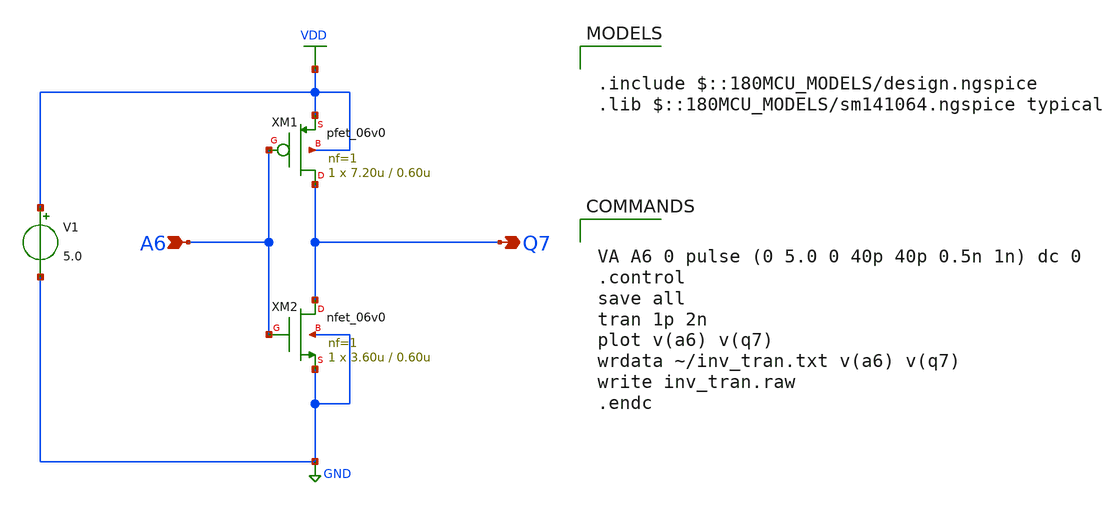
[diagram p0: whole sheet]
** sch_path: member_project/noritsuna/inverter/xschem/inverter_trans.sch
**.subckt inverter_trans A6 Q7
*.ipin A6
*.opin Q7
XM1 Q7 A6 VDD VDD pfet_06v0 L=0.60u W=7.20u nf=1 ad='int((nf+1)/2) * W/nf * 0.18u' as='int((nf+2)/2) * W/nf * 0.18u'
+ pd='2*int((nf+1)/2) * (W/nf + 0.18u)' ps='2*int((nf+2)/2) * (W/nf + 0.18u)' nrd='0.18u / W' nrs='0.18u / W'
+ sa=0 sb=0 sd=0 m=1
XM2 Q7 A6 GND GND nfet_06v0 L=0.60u W=3.60u nf=1 ad='int((nf+1)/2) * W/nf * 0.18u' as='int((nf+2)/2) * W/nf * 0.18u'
+ pd='2*int((nf+1)/2) * (W/nf + 0.18u)' ps='2*int((nf+2)/2) * (W/nf + 0.18u)' nrd='0.18u / W' nrs='0.18u / W'
+ sa=0 sb=0 sd=0 m=1
V1 VDD GND 5.0
**** begin user architecture code

.include $::180MCU_MODELS/design.ngspice
.lib $::180MCU_MODELS/sm141064.ngspice typical



VA A6 0 pulse (0 5.0 0 40p 40p 0.5n 1n) dc 0
.control
save all
tran 1p 2n
plot v(a6) v(q7)
wrdata ~/inv_tran.txt v(a6) v(q7)
write inv_tran.raw
.endc


**** end user architecture code
**.ends
.GLOBAL GND
.GLOBAL VDD
.end
